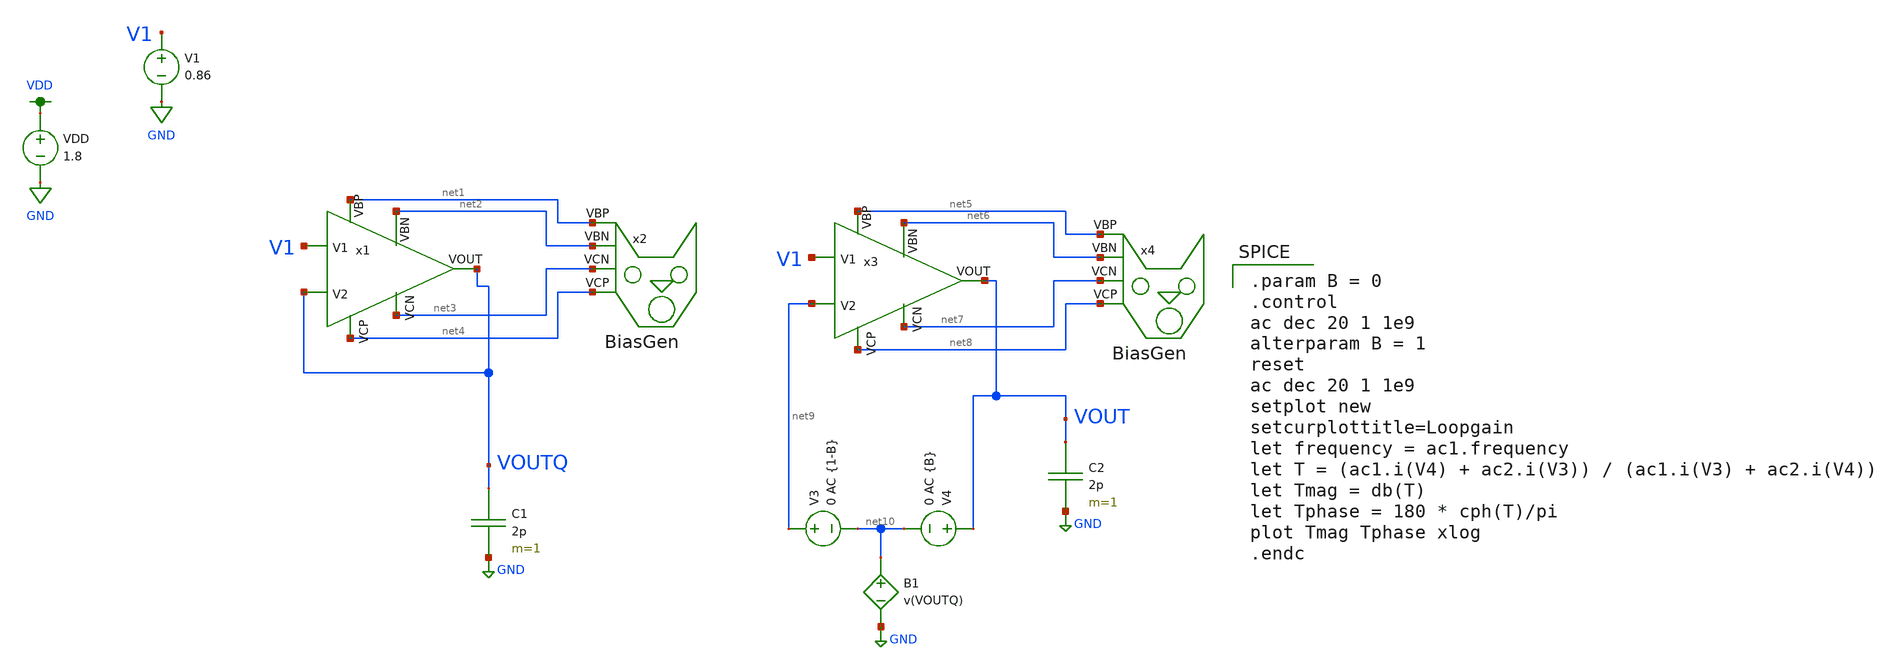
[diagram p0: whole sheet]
** sch_path: MP3/test_harness_loopgain_sim.sch
**.subckt test_harness_loopgain_sim
x1 net1 net4 VOUTQ VOUTQ V1 net3 net2 FCDA
x2 net1 net4 net3 net2 BiasGen
V1 V1 GND 0.86
VDD VDD GND 1.8
C1 VOUTQ GND 2p m=1
x3 net5 net8 net9 VOUT V1 net7 net6 FCDA
x4 net5 net8 net7 net6 BiasGen
C2 VOUT GND 2p m=1
V3 net9 net10 0 AC {1-B}
V4 VOUT net10 0 AC {B}
B1 net10 GND V=v(VOUTQ)
**** begin user architecture code

.option wnflag=1
.lib ~/skywater/skywater-pdk/libraries/sky130_fd_pr_ngspice/latest/models/sky130.lib.spice tt


.param B = 0
.control
ac dec 20 1 1e9
alterparam B = 1
reset
ac dec 20 1 1e9
setplot new
setcurplottitle=Loopgain
let frequency = ac1.frequency
let T = (ac1.i(V4) + ac2.i(V3)) / (ac1.i(V3) + ac2.i(V4))
let Tmag = db(T)
let Tphase = 180 * cph(T)/pi
plot Tmag Tphase xlog
.endc

**** end user architecture code
**.ends

* expanding   symbol:  /home/madvlsi/Documents/MP3/FCDA.sym # of pins=7
** sym_path: MP3/FCDA.sym
** sch_path: MP3/FCDA.sch
.subckt FCDA VBP VCP V2 VOUT V1 VCN VBN
*.ipin V2
*.ipin V1
*.ipin VBN
*.ipin VCN
*.ipin VCP
*.ipin VBP
*.opin VOUT
XM1 net2 V1 net1 GND sky130_fd_pr__nfet_01v8 L=0.5 W=12 nf=1 ad='int((nf+1)/2) * W/nf * 0.29' as='int((nf+2)/2) * W/nf * 0.29'
+ pd='2*int((nf+1)/2) * (W/nf + 0.29)' ps='2*int((nf+2)/2) * (W/nf + 0.29)' nrd='0.29 / W' nrs='0.29 / W'
+ sa=0 sb=0 sd=0 mult=1 m=1
XM2 net3 V2 net1 GND sky130_fd_pr__nfet_01v8 L=0.5 W=12 nf=1 ad='int((nf+1)/2) * W/nf * 0.29' as='int((nf+2)/2) * W/nf * 0.29'
+ pd='2*int((nf+1)/2) * (W/nf + 0.29)' ps='2*int((nf+2)/2) * (W/nf + 0.29)' nrd='0.29 / W' nrs='0.29 / W'
+ sa=0 sb=0 sd=0 mult=1 m=1
XM3 net2 VBP VDD VDD sky130_fd_pr__pfet_01v8 L=0.5 W=12 nf=1 ad='int((nf+1)/2) * W/nf * 0.29' as='int((nf+2)/2) * W/nf * 0.29'
+ pd='2*int((nf+1)/2) * (W/nf + 0.29)' ps='2*int((nf+2)/2) * (W/nf + 0.29)' nrd='0.29 / W' nrs='0.29 / W'
+ sa=0 sb=0 sd=0 mult=1 m=1
XM4 net3 VBP VDD VDD sky130_fd_pr__pfet_01v8 L=0.5 W=12 nf=1 ad='int((nf+1)/2) * W/nf * 0.29' as='int((nf+2)/2) * W/nf * 0.29'
+ pd='2*int((nf+1)/2) * (W/nf + 0.29)' ps='2*int((nf+2)/2) * (W/nf + 0.29)' nrd='0.29 / W' nrs='0.29 / W'
+ sa=0 sb=0 sd=0 mult=1 m=1
XM5 net4 VCP net2 VDD sky130_fd_pr__pfet_01v8 L=0.5 W=12 nf=1 ad='int((nf+1)/2) * W/nf * 0.29' as='int((nf+2)/2) * W/nf * 0.29'
+ pd='2*int((nf+1)/2) * (W/nf + 0.29)' ps='2*int((nf+2)/2) * (W/nf + 0.29)' nrd='0.29 / W' nrs='0.29 / W'
+ sa=0 sb=0 sd=0 mult=1 m=1
XM6 VOUT VCP net3 VDD sky130_fd_pr__pfet_01v8 L=0.5 W=12 nf=1 ad='int((nf+1)/2) * W/nf * 0.29' as='int((nf+2)/2) * W/nf * 0.29'
+ pd='2*int((nf+1)/2) * (W/nf + 0.29)' ps='2*int((nf+2)/2) * (W/nf + 0.29)' nrd='0.29 / W' nrs='0.29 / W'
+ sa=0 sb=0 sd=0 mult=1 m=1
XM7 net5 net4 GND GND sky130_fd_pr__nfet_01v8 L=0.5 W=12 nf=1 ad='int((nf+1)/2) * W/nf * 0.29' as='int((nf+2)/2) * W/nf * 0.29'
+ pd='2*int((nf+1)/2) * (W/nf + 0.29)' ps='2*int((nf+2)/2) * (W/nf + 0.29)' nrd='0.29 / W' nrs='0.29 / W'
+ sa=0 sb=0 sd=0 mult=1 m=1
XM8 net6 net4 GND GND sky130_fd_pr__nfet_01v8 L=0.5 W=12 nf=1 ad='int((nf+1)/2) * W/nf * 0.29' as='int((nf+2)/2) * W/nf * 0.29'
+ pd='2*int((nf+1)/2) * (W/nf + 0.29)' ps='2*int((nf+2)/2) * (W/nf + 0.29)' nrd='0.29 / W' nrs='0.29 / W'
+ sa=0 sb=0 sd=0 mult=1 m=1
XM9 net4 VCN net5 GND sky130_fd_pr__nfet_01v8 L=0.5 W=12 nf=1 ad='int((nf+1)/2) * W/nf * 0.29' as='int((nf+2)/2) * W/nf * 0.29'
+ pd='2*int((nf+1)/2) * (W/nf + 0.29)' ps='2*int((nf+2)/2) * (W/nf + 0.29)' nrd='0.29 / W' nrs='0.29 / W'
+ sa=0 sb=0 sd=0 mult=1 m=1
XM10 VOUT VCN net6 GND sky130_fd_pr__nfet_01v8 L=0.5 W=12 nf=1 ad='int((nf+1)/2) * W/nf * 0.29' as='int((nf+2)/2) * W/nf * 0.29'
+ pd='2*int((nf+1)/2) * (W/nf + 0.29)' ps='2*int((nf+2)/2) * (W/nf + 0.29)' nrd='0.29 / W' nrs='0.29 / W'
+ sa=0 sb=0 sd=0 mult=1 m=1
XMb net1 VBN GND GND sky130_fd_pr__nfet_01v8 L=0.5 W=12 nf=1 ad='int((nf+1)/2) * W/nf * 0.29' as='int((nf+2)/2) * W/nf * 0.29'
+ pd='2*int((nf+1)/2) * (W/nf + 0.29)' ps='2*int((nf+2)/2) * (W/nf + 0.29)' nrd='0.29 / W' nrs='0.29 / W'
+ sa=0 sb=0 sd=0 mult=1 m=1
.ends


* expanding   symbol:  /home/madvlsi/Documents/MP3/BiasGen.sym # of pins=4
** sym_path: MP3/BiasGen.sym
** sch_path: MP3/BiasGen.sch
.subckt BiasGen VBP VCP VCN VBN
*.opin VCN
*.opin VCP
*.opin VBP
*.opin VBN
XM1 net1 net1 net2 GND sky130_fd_pr__nfet_01v8 L=0.5 W=48 nf=1 ad='int((nf+1)/2) * W/nf * 0.29' as='int((nf+2)/2) * W/nf * 0.29'
+ pd='2*int((nf+1)/2) * (W/nf + 0.29)' ps='2*int((nf+2)/2) * (W/nf + 0.29)' nrd='0.29 / W' nrs='0.29 / W'
+ sa=0 sb=0 sd=0 mult=1 m=1
XM2 net2 net1 GND GND sky130_fd_pr__nfet_01v8 L=0.5 W=12 nf=1 ad='int((nf+1)/2) * W/nf * 0.29' as='int((nf+2)/2) * W/nf * 0.29'
+ pd='2*int((nf+1)/2) * (W/nf + 0.29)' ps='2*int((nf+2)/2) * (W/nf + 0.29)' nrd='0.29 / W' nrs='0.29 / W'
+ sa=0 sb=0 sd=0 mult=1 m=1
XM3 VCN VCN net2 GND sky130_fd_pr__nfet_01v8 L=0.5 W=12 nf=1 ad='int((nf+1)/2) * W/nf * 0.29' as='int((nf+2)/2) * W/nf * 0.29'
+ pd='2*int((nf+1)/2) * (W/nf + 0.29)' ps='2*int((nf+2)/2) * (W/nf + 0.29)' nrd='0.29 / W' nrs='0.29 / W'
+ sa=0 sb=0 sd=0 mult=1 m=1
XM4 net1 VBP VDD VDD sky130_fd_pr__pfet_01v8 L=2.5 W=12 nf=1 ad='int((nf+1)/2) * W/nf * 0.29' as='int((nf+2)/2) * W/nf * 0.29'
+ pd='2*int((nf+1)/2) * (W/nf + 0.29)' ps='2*int((nf+2)/2) * (W/nf + 0.29)' nrd='0.29 / W' nrs='0.29 / W'
+ sa=0 sb=0 sd=0 mult=1 m=1
XM5 VCN VBP VDD VDD sky130_fd_pr__pfet_01v8 L=0.5 W=12 nf=1 ad='int((nf+1)/2) * W/nf * 0.29' as='int((nf+2)/2) * W/nf * 0.29'
+ pd='2*int((nf+1)/2) * (W/nf + 0.29)' ps='2*int((nf+2)/2) * (W/nf + 0.29)' nrd='0.29 / W' nrs='0.29 / W'
+ sa=0 sb=0 sd=0 mult=1 m=1
XM6 net4 net3 VDD VDD sky130_fd_pr__pfet_01v8 L=0.5 W=12 nf=1 ad='int((nf+1)/2) * W/nf * 0.29' as='int((nf+2)/2) * W/nf * 0.29'
+ pd='2*int((nf+1)/2) * (W/nf + 0.29)' ps='2*int((nf+2)/2) * (W/nf + 0.29)' nrd='0.29 / W' nrs='0.29 / W'
+ sa=0 sb=0 sd=0 mult=1 m=1
XM7 net3 net3 net4 VDD sky130_fd_pr__pfet_01v8 L=0.5 W=48 nf=1 ad='int((nf+1)/2) * W/nf * 0.29' as='int((nf+2)/2) * W/nf * 0.29'
+ pd='2*int((nf+1)/2) * (W/nf + 0.29)' ps='2*int((nf+2)/2) * (W/nf + 0.29)' nrd='0.29 / W' nrs='0.29 / W'
+ sa=0 sb=0 sd=0 mult=1 m=1
XM8 VCP VCP net4 VDD sky130_fd_pr__pfet_01v8 L=0.5 W=12 nf=1 ad='int((nf+1)/2) * W/nf * 0.29' as='int((nf+2)/2) * W/nf * 0.29'
+ pd='2*int((nf+1)/2) * (W/nf + 0.29)' ps='2*int((nf+2)/2) * (W/nf + 0.29)' nrd='0.29 / W' nrs='0.29 / W'
+ sa=0 sb=0 sd=0 mult=1 m=1
XM9 net3 VBN GND GND sky130_fd_pr__nfet_01v8 L=2.5 W=12 nf=1 ad='int((nf+1)/2) * W/nf * 0.29' as='int((nf+2)/2) * W/nf * 0.29'
+ pd='2*int((nf+1)/2) * (W/nf + 0.29)' ps='2*int((nf+2)/2) * (W/nf + 0.29)' nrd='0.29 / W' nrs='0.29 / W'
+ sa=0 sb=0 sd=0 mult=1 m=1
XM10 VCP VBN GND GND sky130_fd_pr__nfet_01v8 L=0.5 W=12 nf=1 ad='int((nf+1)/2) * W/nf * 0.29' as='int((nf+2)/2) * W/nf * 0.29'
+ pd='2*int((nf+1)/2) * (W/nf + 0.29)' ps='2*int((nf+2)/2) * (W/nf + 0.29)' nrd='0.29 / W' nrs='0.29 / W'
+ sa=0 sb=0 sd=0 mult=1 m=1
XM11 VBP VBP VDD VDD sky130_fd_pr__pfet_01v8 L=0.5 W=12 nf=1 ad='int((nf+1)/2) * W/nf * 0.29' as='int((nf+2)/2) * W/nf * 0.29'
+ pd='2*int((nf+1)/2) * (W/nf + 0.29)' ps='2*int((nf+2)/2) * (W/nf + 0.29)' nrd='0.29 / W' nrs='0.29 / W'
+ sa=0 sb=0 sd=0 mult=1 m=1
XM12 VBP VBN GND GND sky130_fd_pr__nfet_01v8 L=0.5 W=12 nf=1 ad='int((nf+1)/2) * W/nf * 0.29' as='int((nf+2)/2) * W/nf * 0.29'
+ pd='2*int((nf+1)/2) * (W/nf + 0.29)' ps='2*int((nf+2)/2) * (W/nf + 0.29)' nrd='0.29 / W' nrs='0.29 / W'
+ sa=0 sb=0 sd=0 mult=1 m=1
XM13 VBN VBN GND GND sky130_fd_pr__nfet_01v8 L=0.5 W=12 nf=1 ad='int((nf+1)/2) * W/nf * 0.29' as='int((nf+2)/2) * W/nf * 0.29'
+ pd='2*int((nf+1)/2) * (W/nf + 0.29)' ps='2*int((nf+2)/2) * (W/nf + 0.29)' nrd='0.29 / W' nrs='0.29 / W'
+ sa=0 sb=0 sd=0 mult=1 m=1
IB GND VBN 1u
.ends

.GLOBAL GND
.GLOBAL VDD
.end
